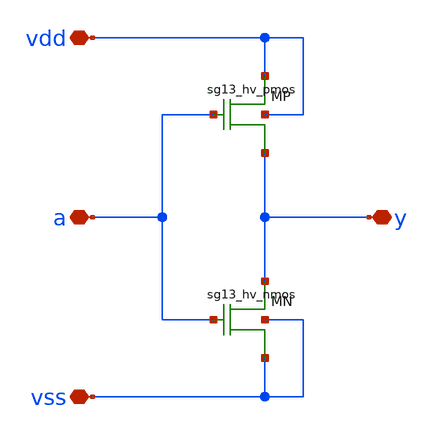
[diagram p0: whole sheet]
** sch_path: xschem/logic_gates/INVHV1S.sch
**.subckt INVHV1S vdd vss y a
*.iopin vdd
*.iopin vss
*.iopin y
*.iopin a
XMP vdd a y vdd sg13_hv_pmos w=2.0u l=0.45u ng=1 m=1
XMN y a vss vss sg13_hv_nmos w=2.0u l=0.45u ng=1 m=1
**.ends
.end
